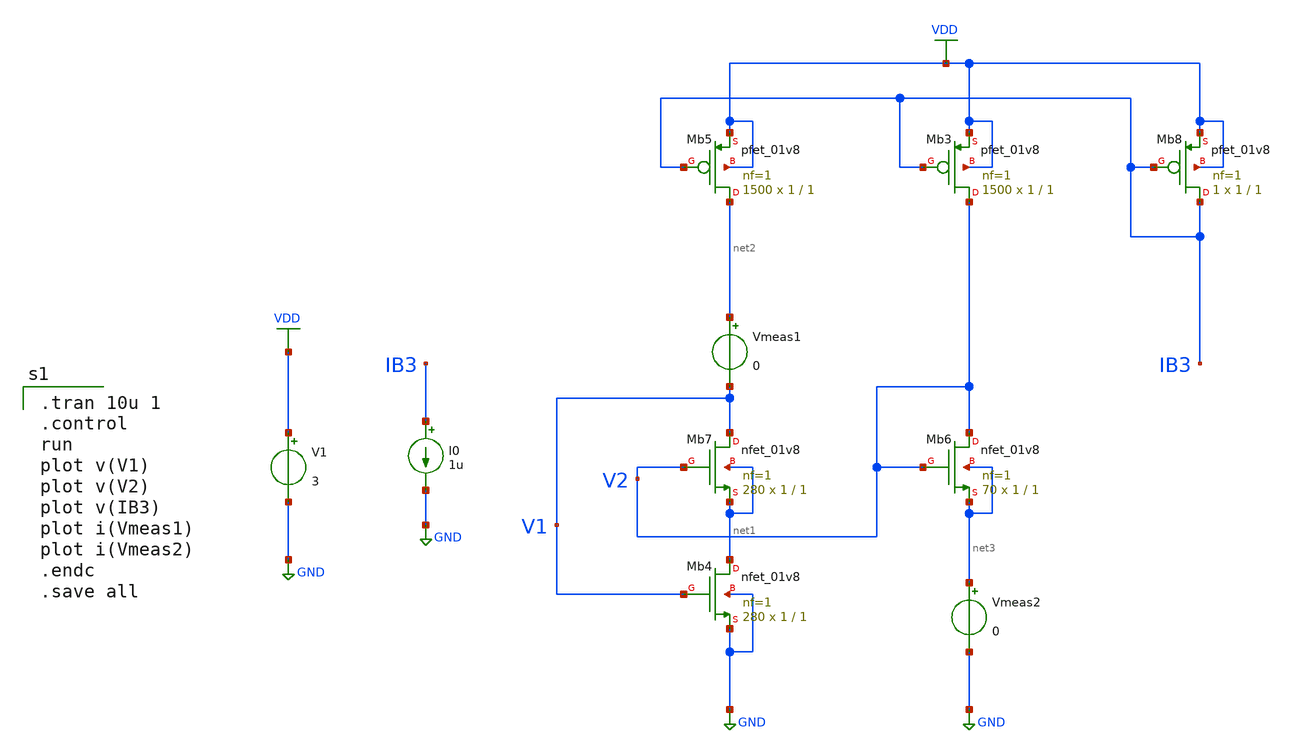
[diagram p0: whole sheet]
** sch_path: Circuits/Examples/Analog/Trans_Testing/NMOS_Test.sch
**.subckt NMOS_Test
V1 VDD GND 3
XMb4 net1 V1 GND GND sky130_fd_pr__nfet_01v8 L=1 W=1 nf=1 ad='int((nf+1)/2) * W/nf * 0.29' as='int((nf+2)/2) * W/nf * 0.29'
+ pd='2*int((nf+1)/2) * (W/nf + 0.29)' ps='2*int((nf+2)/2) * (W/nf + 0.29)' nrd='0.29 / W' nrs='0.29 / W'
+ sa=0 sb=0 sd=0 mult=280 m=280
XMb7 V1 V2 net1 net1 sky130_fd_pr__nfet_01v8 L=1 W=1 nf=1 ad='int((nf+1)/2) * W/nf * 0.29' as='int((nf+2)/2) * W/nf * 0.29'
+ pd='2*int((nf+1)/2) * (W/nf + 0.29)' ps='2*int((nf+2)/2) * (W/nf + 0.29)' nrd='0.29 / W' nrs='0.29 / W'
+ sa=0 sb=0 sd=0 mult=280 m=280
XMb5 net2 IB3 VDD VDD sky130_fd_pr__pfet_01v8 L=1 W=1 nf=1 ad='int((nf+1)/2) * W/nf * 0.29' as='int((nf+2)/2) * W/nf * 0.29'
+ pd='2*int((nf+1)/2) * (W/nf + 0.29)' ps='2*int((nf+2)/2) * (W/nf + 0.29)' nrd='0.29 / W' nrs='0.29 / W'
+ sa=0 sb=0 sd=0 mult=1500 m=1500
XMb3 V2 IB3 VDD VDD sky130_fd_pr__pfet_01v8 L=1 W=1 nf=1 ad='int((nf+1)/2) * W/nf * 0.29' as='int((nf+2)/2) * W/nf * 0.29'
+ pd='2*int((nf+1)/2) * (W/nf + 0.29)' ps='2*int((nf+2)/2) * (W/nf + 0.29)' nrd='0.29 / W' nrs='0.29 / W'
+ sa=0 sb=0 sd=0 mult=1500 m=1500
XMb6 V2 V2 net3 net3 sky130_fd_pr__nfet_01v8 L=1 W=1 nf=1 ad='int((nf+1)/2) * W/nf * 0.29' as='int((nf+2)/2) * W/nf * 0.29'
+ pd='2*int((nf+1)/2) * (W/nf + 0.29)' ps='2*int((nf+2)/2) * (W/nf + 0.29)' nrd='0.29 / W' nrs='0.29 / W'
+ sa=0 sb=0 sd=0 mult=70 m=70
XMb8 IB3 IB3 VDD VDD sky130_fd_pr__pfet_01v8 L=1 W=1 nf=1 ad='int((nf+1)/2) * W/nf * 0.29' as='int((nf+2)/2) * W/nf * 0.29'
+ pd='2*int((nf+1)/2) * (W/nf + 0.29)' ps='2*int((nf+2)/2) * (W/nf + 0.29)' nrd='0.29 / W' nrs='0.29 / W'
+ sa=0 sb=0 sd=0 mult=1 m=1
I0 IB3 GND 1u
Vmeas1 net2 V1 0
Vmeas2 net3 GND 0
**** begin user architecture code
 ** manual skywater pdks install (with patches applied)
* .lib $::SKYWATER_MODELS/models/sky130.lib.spice tt

** opencircuitdesign pdks install
.lib $::SKYWATER_MODELS/sky130.lib.spice tt

.param mc_mm_switch=0
.param mc_pr_switch=0


.tran 10u 1
.control
run
plot v(V1)
plot v(V2)
plot v(IB3)
plot i(Vmeas1)
plot i(Vmeas2)
.endc
.save all

**** end user architecture code
**.ends
.GLOBAL GND
.GLOBAL VDD
.end
